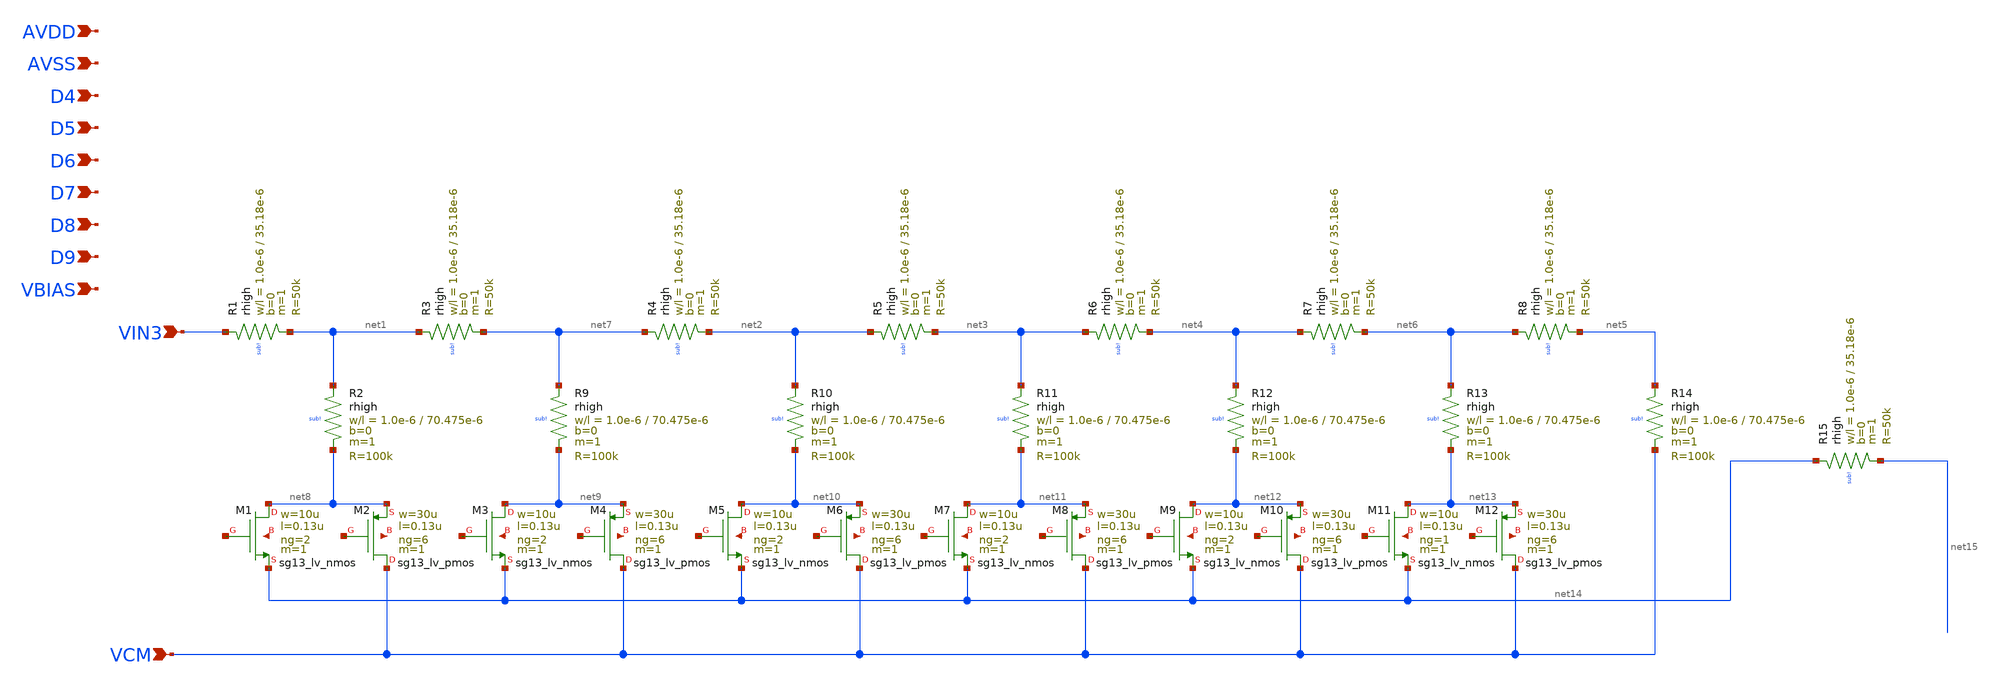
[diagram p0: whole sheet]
** sch_path: designs/libs/core_analog/fine_gain/fine_gain.sch
**.subckt fine_gain AVSS VIN3 VCM D4 D5 D6 D7 D8 D9 AVDD VBIAS
*.ipin AVSS
*.ipin VIN3
*.ipin VCM
*.ipin D4
*.ipin D5
*.ipin D6
*.ipin D7
*.ipin D8
*.ipin D9
*.ipin AVDD
*.ipin VBIAS
XR1 VIN3 net1 sub! rhigh w=1.0e-6 l=35.18e-6 m=1 b=0 mm_ok=1
XR2 net1 net8 sub! rhigh w=1.0e-6 l=70.475e-6 m=1 b=0 mm_ok=1
XR3 net1 net7 sub! rhigh w=1.0e-6 l=35.18e-6 m=1 b=0 mm_ok=1
XR4 net7 net2 sub! rhigh w=1.0e-6 l=35.18e-6 m=1 b=0 mm_ok=1
XR5 net2 net3 sub! rhigh w=1.0e-6 l=35.18e-6 m=1 b=0 mm_ok=1
XR6 net3 net4 sub! rhigh w=1.0e-6 l=35.18e-6 m=1 b=0 mm_ok=1
XR7 net4 net6 sub! rhigh w=1.0e-6 l=35.18e-6 m=1 b=0 mm_ok=1
XR8 net6 net5 sub! rhigh w=1.0e-6 l=35.18e-6 m=1 b=0 mm_ok=1
XR9 net7 net9 sub! rhigh w=1.0e-6 l=70.475e-6 m=1 b=0 mm_ok=1
XR10 net2 net10 sub! rhigh w=1.0e-6 l=70.475e-6 m=1 b=0 mm_ok=1
XR11 net3 net11 sub! rhigh w=1.0e-6 l=70.475e-6 m=1 b=0 mm_ok=1
XR12 net4 net12 sub! rhigh w=1.0e-6 l=70.475e-6 m=1 b=0 mm_ok=1
XR13 net6 net13 sub! rhigh w=1.0e-6 l=70.475e-6 m=1 b=0 mm_ok=1
XR14 net5 VCM sub! rhigh w=1.0e-6 l=70.475e-6 m=1 b=0 mm_ok=1
XM1 net8 net16 net14 net17 sg13_lv_nmos w=10u l=0.13u ng=2 m=1 mm_ok=1
XM2 VCM net18 net8 net19 sg13_lv_pmos w=30u l=0.13u ng=6 m=1 mm_ok=1
XM3 net9 net20 net14 net21 sg13_lv_nmos w=10u l=0.13u ng=2 m=1 mm_ok=1
XM4 VCM net22 net9 net23 sg13_lv_pmos w=30u l=0.13u ng=6 m=1 mm_ok=1
XM5 net10 net24 net14 net25 sg13_lv_nmos w=10u l=0.13u ng=2 m=1 mm_ok=1
XM6 VCM net26 net10 net27 sg13_lv_pmos w=30u l=0.13u ng=6 m=1 mm_ok=1
XM7 net11 net28 net14 net29 sg13_lv_nmos w=10u l=0.13u ng=2 m=1 mm_ok=1
XM8 VCM net30 net11 net31 sg13_lv_pmos w=30u l=0.13u ng=6 m=1 mm_ok=1
XM9 net12 net32 net14 net33 sg13_lv_nmos w=10u l=0.13u ng=2 m=1 mm_ok=1
XM10 VCM net34 net12 net35 sg13_lv_pmos w=30u l=0.13u ng=6 m=1 mm_ok=1
XM11 net13 net36 net14 net37 sg13_lv_nmos w=10u l=0.13u ng=1 m=1 mm_ok=1
XM12 VCM net38 net13 net39 sg13_lv_pmos w=30u l=0.13u ng=6 m=1 mm_ok=1
XR15 net14 net15 sub! rhigh w=1.0e-6 l=35.18e-6 m=1 b=0 mm_ok=1
**.ends
.end
